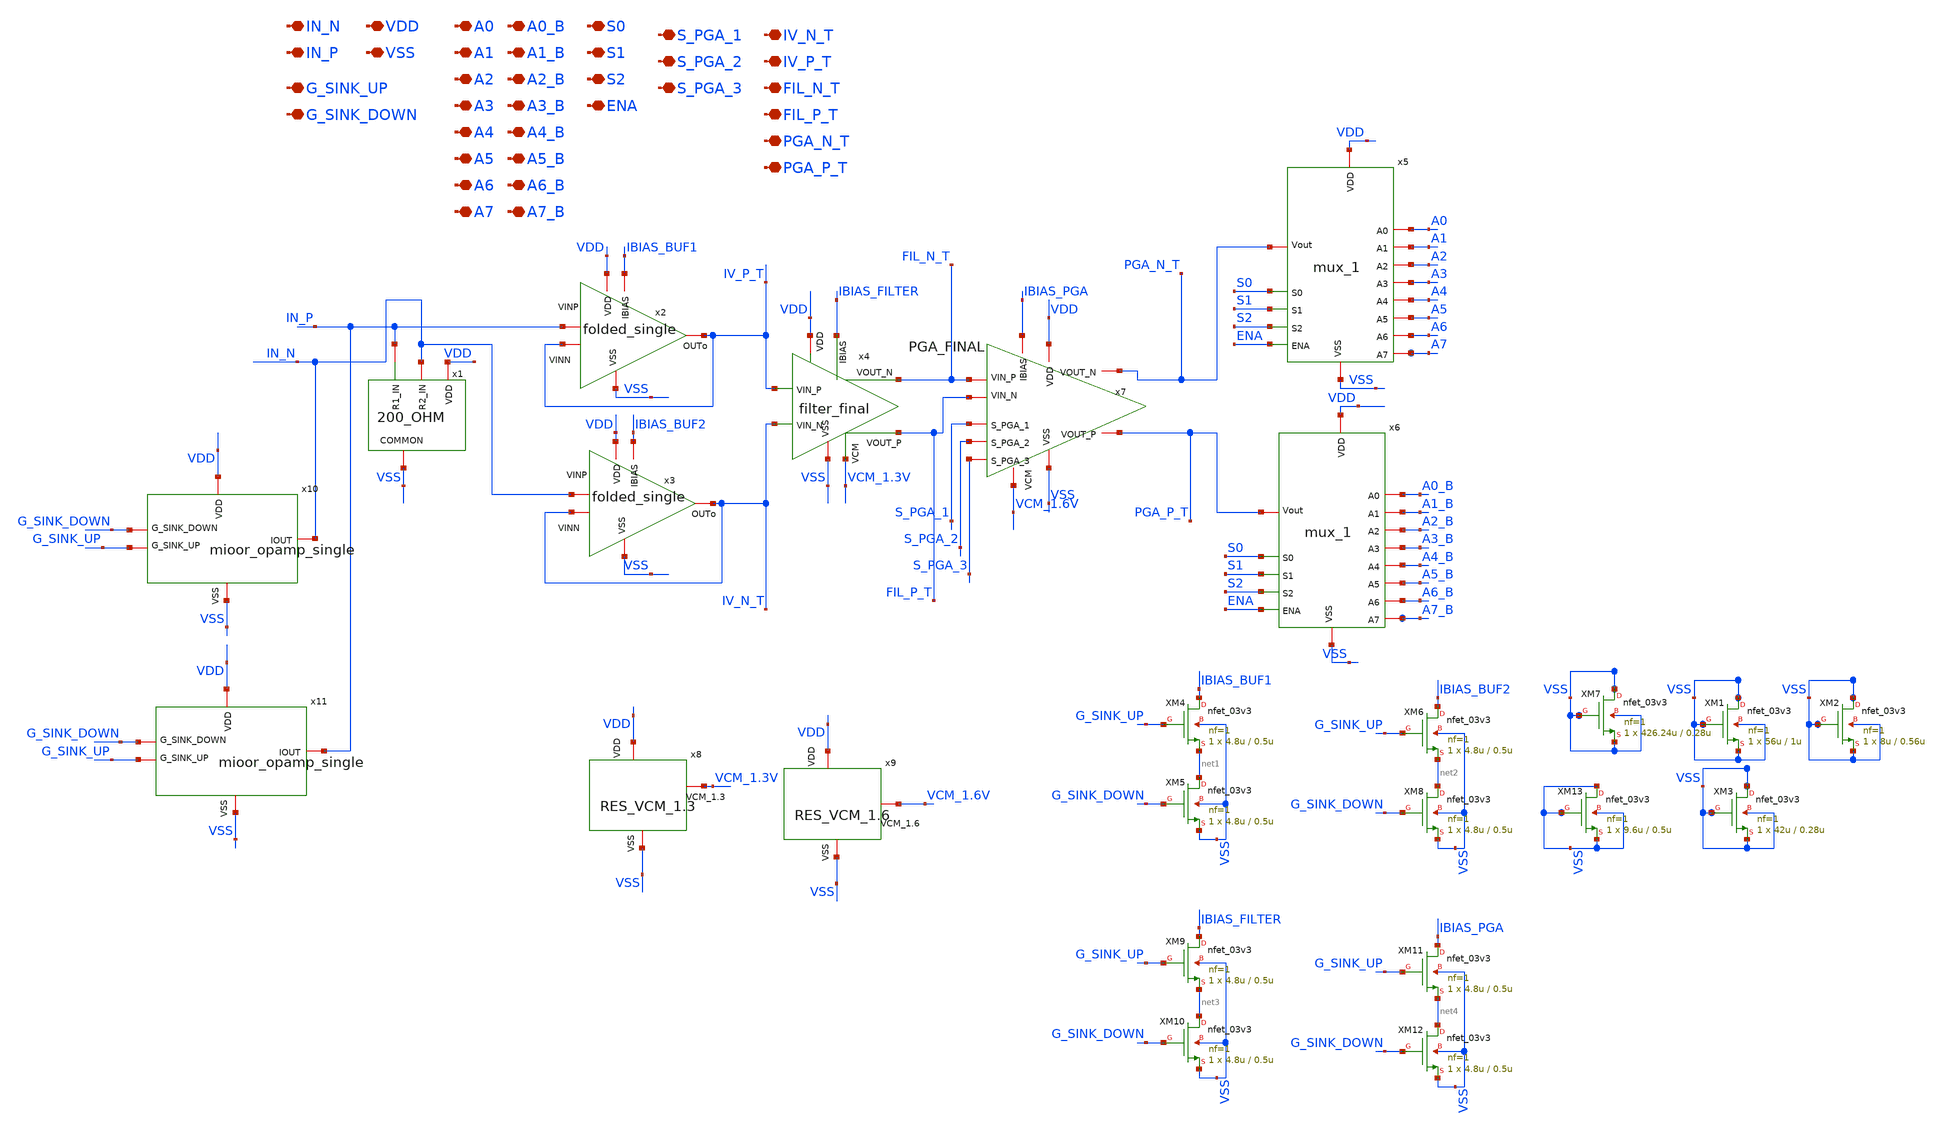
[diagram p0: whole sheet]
** sch_path: AWG_OUTPUT_AND_MUX_PAKISTAN_05/xschem/AWG_MUX_FINAL.sch
**.subckt AWG_MUX_FINAL VDD VSS IN_N IN_P A0 A1 A2 A3 A4 A5 A6 A7 A0_B A1_B A2_B A3_B A4_B A5_B A6_B
*+ A7_B S0 S1 S2 ENA S_PGA_1 S_PGA_2 S_PGA_3 IV_N_T IV_P_T FIL_N_T FIL_P_T PGA_N_T PGA_P_T G_SINK_UP
*+ G_SINK_DOWN
*.iopin VDD
*.iopin VSS
*.iopin IN_N
*.iopin IN_P
*.iopin A0
*.iopin A1
*.iopin A2
*.iopin A3
*.iopin A4
*.iopin A5
*.iopin A6
*.iopin A7
*.iopin A0_B
*.iopin A1_B
*.iopin A2_B
*.iopin A3_B
*.iopin A4_B
*.iopin A5_B
*.iopin A6_B
*.iopin A7_B
*.iopin S0
*.iopin S1
*.iopin S2
*.iopin ENA
*.iopin S_PGA_1
*.iopin S_PGA_2
*.iopin S_PGA_3
*.iopin IV_N_T
*.iopin IV_P_T
*.iopin FIL_N_T
*.iopin FIL_P_T
*.iopin PGA_N_T
*.iopin PGA_P_T
*.iopin G_SINK_UP
*.iopin G_SINK_DOWN
x1 IN_P VSS IN_N VDD 200_OHM
x2 IV_P_T VDD VSS IV_P_T IN_P IBIAS_BUF1 folded_single
x3 IV_N_T VDD VSS IV_N_T IN_N IBIAS_BUF2 folded_single
x4 IV_N_T IV_P_T FIL_P_T FIL_N_T VDD IBIAS_FILTER VCM_1.3V VSS filter_final
x5 VDD PGA_N_T VSS A0 A1 A2 A3 A4 A5 A6 A7 S0 S1 S2 ENA mux_1
x6 VDD PGA_P_T VSS A0_B A1_B A2_B A3_B A4_B A5_B A6_B A7_B S0 S1 S2 ENA mux_1
x7 PGA_N_T FIL_N_T VDD S_PGA_1 VSS FIL_P_T S_PGA_2 PGA_P_T S_PGA_3 IBIAS_PGA VCM_1.6V PGA_FINAL
XM7 VSS VSS VSS VSS nfet_03v3 L=0.28u W=426.24u nf=1 ad='int((nf+1)/2) * W/nf * 0.18u' as='int((nf+2)/2) * W/nf * 0.18u'
+ pd='2*int((nf+1)/2) * (W/nf + 0.18u)' ps='2*int((nf+2)/2) * (W/nf + 0.18u)' nrd='0.18u / W' nrs='0.18u / W'
+ sa=0 sb=0 sd=0 m=1
XM1 VSS VSS VSS VSS nfet_03v3 L=1u W=56u nf=1 ad='int((nf+1)/2) * W/nf * 0.18u' as='int((nf+2)/2) * W/nf * 0.18u'
+ pd='2*int((nf+1)/2) * (W/nf + 0.18u)' ps='2*int((nf+2)/2) * (W/nf + 0.18u)' nrd='0.18u / W' nrs='0.18u / W'
+ sa=0 sb=0 sd=0 m=1
XM2 VSS VSS VSS VSS nfet_03v3 L=0.56u W=8u nf=1 ad='int((nf+1)/2) * W/nf * 0.18u' as='int((nf+2)/2) * W/nf * 0.18u'
+ pd='2*int((nf+1)/2) * (W/nf + 0.18u)' ps='2*int((nf+2)/2) * (W/nf + 0.18u)' nrd='0.18u / W' nrs='0.18u / W'
+ sa=0 sb=0 sd=0 m=1
XM3 VSS VSS VSS VSS nfet_03v3 L=0.28u W=42u nf=1 ad='int((nf+1)/2) * W/nf * 0.18u' as='int((nf+2)/2) * W/nf * 0.18u'
+ pd='2*int((nf+1)/2) * (W/nf + 0.18u)' ps='2*int((nf+2)/2) * (W/nf + 0.18u)' nrd='0.18u / W' nrs='0.18u / W'
+ sa=0 sb=0 sd=0 m=1
XM4 IBIAS_BUF1 G_SINK_UP net1 VSS nfet_03v3 L=0.5u W=4.8u nf=1 ad='int((nf+1)/2) * W/nf * 0.18u' as='int((nf+2)/2) * W/nf * 0.18u'
+ pd='2*int((nf+1)/2) * (W/nf + 0.18u)' ps='2*int((nf+2)/2) * (W/nf + 0.18u)' nrd='0.18u / W' nrs='0.18u / W'
+ sa=0 sb=0 sd=0 m=1
XM5 net1 G_SINK_DOWN VSS VSS nfet_03v3 L=0.5u W=4.8u nf=1 ad='int((nf+1)/2) * W/nf * 0.18u' as='int((nf+2)/2) * W/nf * 0.18u'
+ pd='2*int((nf+1)/2) * (W/nf + 0.18u)' ps='2*int((nf+2)/2) * (W/nf + 0.18u)' nrd='0.18u / W' nrs='0.18u / W'
+ sa=0 sb=0 sd=0 m=1
XM6 IBIAS_BUF2 G_SINK_UP net2 VSS nfet_03v3 L=0.5u W=4.8u nf=1 ad='int((nf+1)/2) * W/nf * 0.18u' as='int((nf+2)/2) * W/nf * 0.18u'
+ pd='2*int((nf+1)/2) * (W/nf + 0.18u)' ps='2*int((nf+2)/2) * (W/nf + 0.18u)' nrd='0.18u / W' nrs='0.18u / W'
+ sa=0 sb=0 sd=0 m=1
XM8 net2 G_SINK_DOWN VSS VSS nfet_03v3 L=0.5u W=4.8u nf=1 ad='int((nf+1)/2) * W/nf * 0.18u' as='int((nf+2)/2) * W/nf * 0.18u'
+ pd='2*int((nf+1)/2) * (W/nf + 0.18u)' ps='2*int((nf+2)/2) * (W/nf + 0.18u)' nrd='0.18u / W' nrs='0.18u / W'
+ sa=0 sb=0 sd=0 m=1
XM9 IBIAS_FILTER G_SINK_UP net3 VSS nfet_03v3 L=0.5u W=4.8u nf=1 ad='int((nf+1)/2) * W/nf * 0.18u' as='int((nf+2)/2) * W/nf * 0.18u'
+ pd='2*int((nf+1)/2) * (W/nf + 0.18u)' ps='2*int((nf+2)/2) * (W/nf + 0.18u)' nrd='0.18u / W' nrs='0.18u / W'
+ sa=0 sb=0 sd=0 m=1
XM10 net3 G_SINK_DOWN VSS VSS nfet_03v3 L=0.5u W=4.8u nf=1 ad='int((nf+1)/2) * W/nf * 0.18u' as='int((nf+2)/2) * W/nf * 0.18u'
+ pd='2*int((nf+1)/2) * (W/nf + 0.18u)' ps='2*int((nf+2)/2) * (W/nf + 0.18u)' nrd='0.18u / W' nrs='0.18u / W'
+ sa=0 sb=0 sd=0 m=1
XM11 IBIAS_PGA G_SINK_UP net4 VSS nfet_03v3 L=0.5u W=4.8u nf=1 ad='int((nf+1)/2) * W/nf * 0.18u' as='int((nf+2)/2) * W/nf * 0.18u'
+ pd='2*int((nf+1)/2) * (W/nf + 0.18u)' ps='2*int((nf+2)/2) * (W/nf + 0.18u)' nrd='0.18u / W' nrs='0.18u / W'
+ sa=0 sb=0 sd=0 m=1
XM12 net4 G_SINK_DOWN VSS VSS nfet_03v3 L=0.5u W=4.8u nf=1 ad='int((nf+1)/2) * W/nf * 0.18u' as='int((nf+2)/2) * W/nf * 0.18u'
+ pd='2*int((nf+1)/2) * (W/nf + 0.18u)' ps='2*int((nf+2)/2) * (W/nf + 0.18u)' nrd='0.18u / W' nrs='0.18u / W'
+ sa=0 sb=0 sd=0 m=1
x8 VSS VCM_1.3V VDD RES_VCM_1.3
x9 VCM_1.6V VSS VDD RES_VCM_1.6
XM13 VSS VSS VSS VSS nfet_03v3 L=0.5u W=9.6u nf=1 ad='int((nf+1)/2) * W/nf * 0.18u' as='int((nf+2)/2) * W/nf * 0.18u'
+ pd='2*int((nf+1)/2) * (W/nf + 0.18u)' ps='2*int((nf+2)/2) * (W/nf + 0.18u)' nrd='0.18u / W' nrs='0.18u / W'
+ sa=0 sb=0 sd=0 m=1
x10 VDD VSS G_SINK_UP G_SINK_DOWN IN_N mioor_opamp_single
x11 VDD VSS G_SINK_UP G_SINK_DOWN IN_P mioor_opamp_single
**.ends
.end
